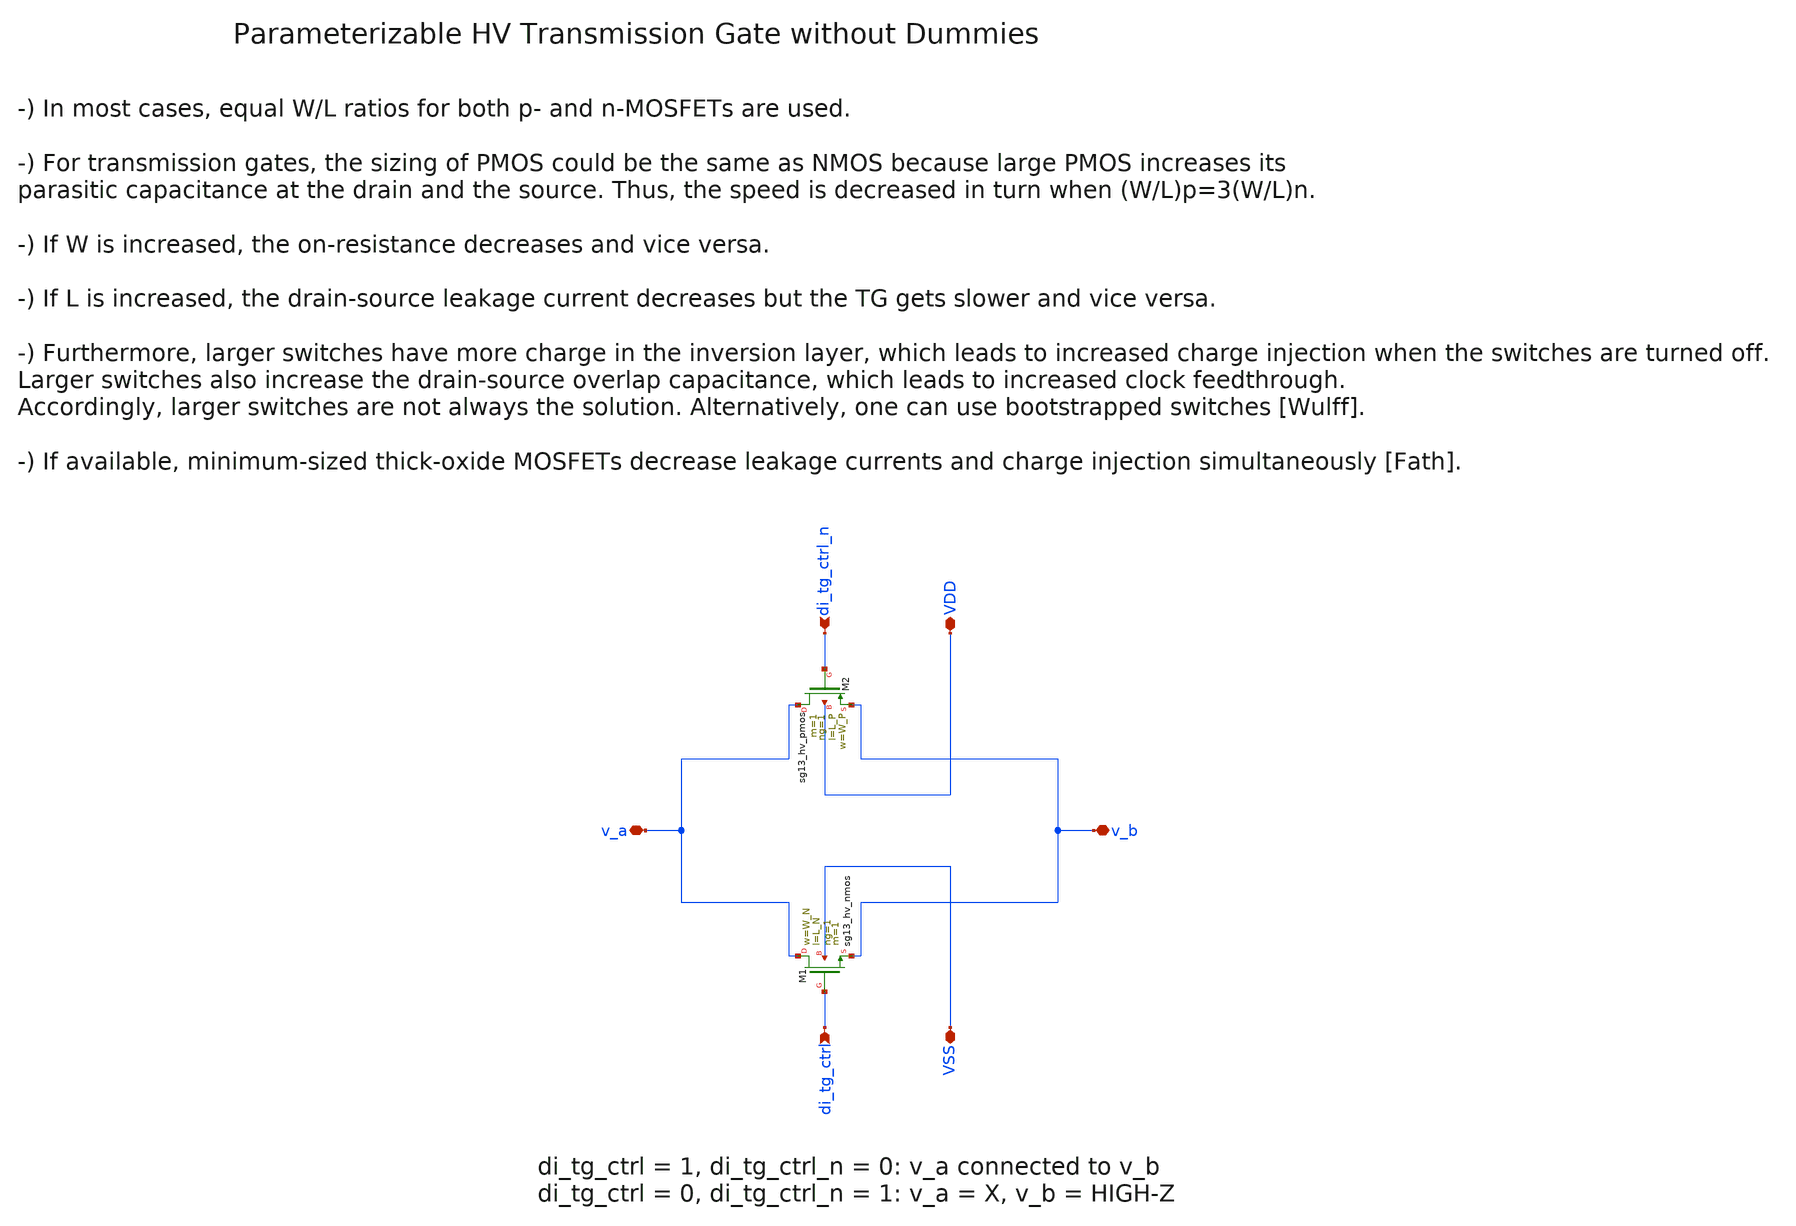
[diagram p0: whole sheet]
** sch_path: SG13G2_ATBS-ADC-main/xschem/transmission_gate/transmission_gate_hv_wo_dummy.sch
**.subckt transmission_gate_hv_wo_dummy v_a v_b VDD VSS di_tg_ctrl di_tg_ctrl_n
*.iopin v_a
*.iopin v_b
*.iopin VDD
*.iopin VSS
*.ipin di_tg_ctrl
*.ipin di_tg_ctrl_n
XM1 v_a di_tg_ctrl v_b VSS sg13_hv_nmos w=W_N l=L_N ng=1 m=1 mm_ok=1
XM2 v_a di_tg_ctrl_n v_b VDD sg13_hv_pmos w=W_P l=L_P ng=1 m=1 mm_ok=1
**.ends
.end
